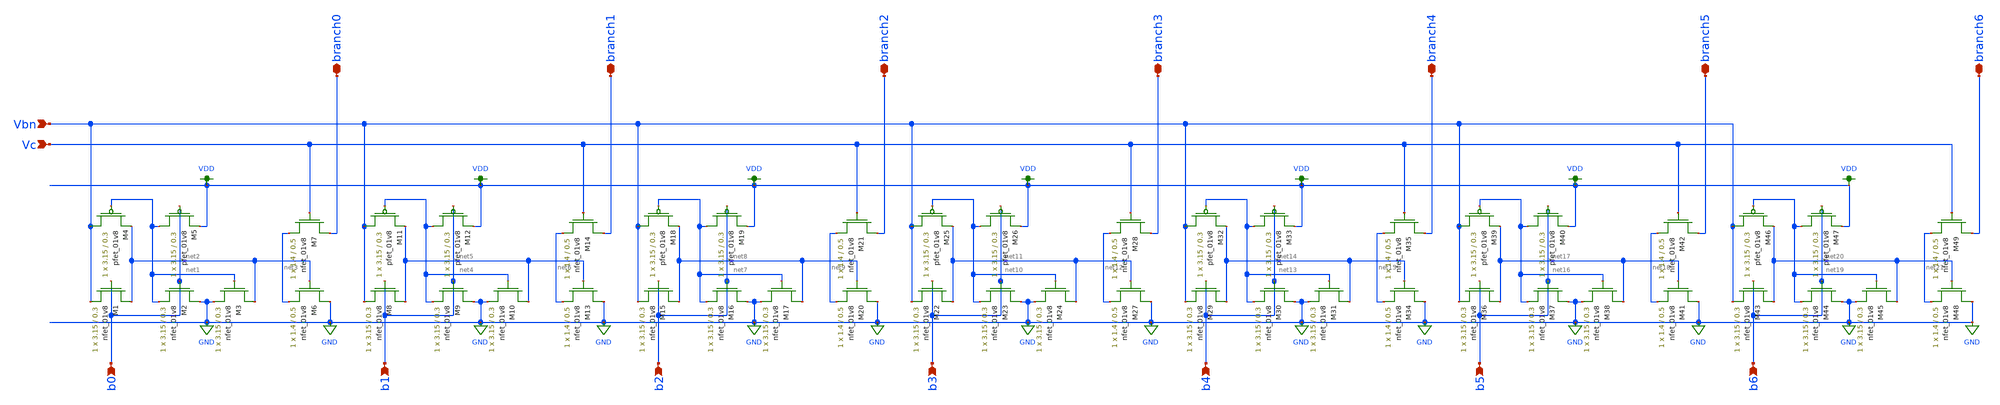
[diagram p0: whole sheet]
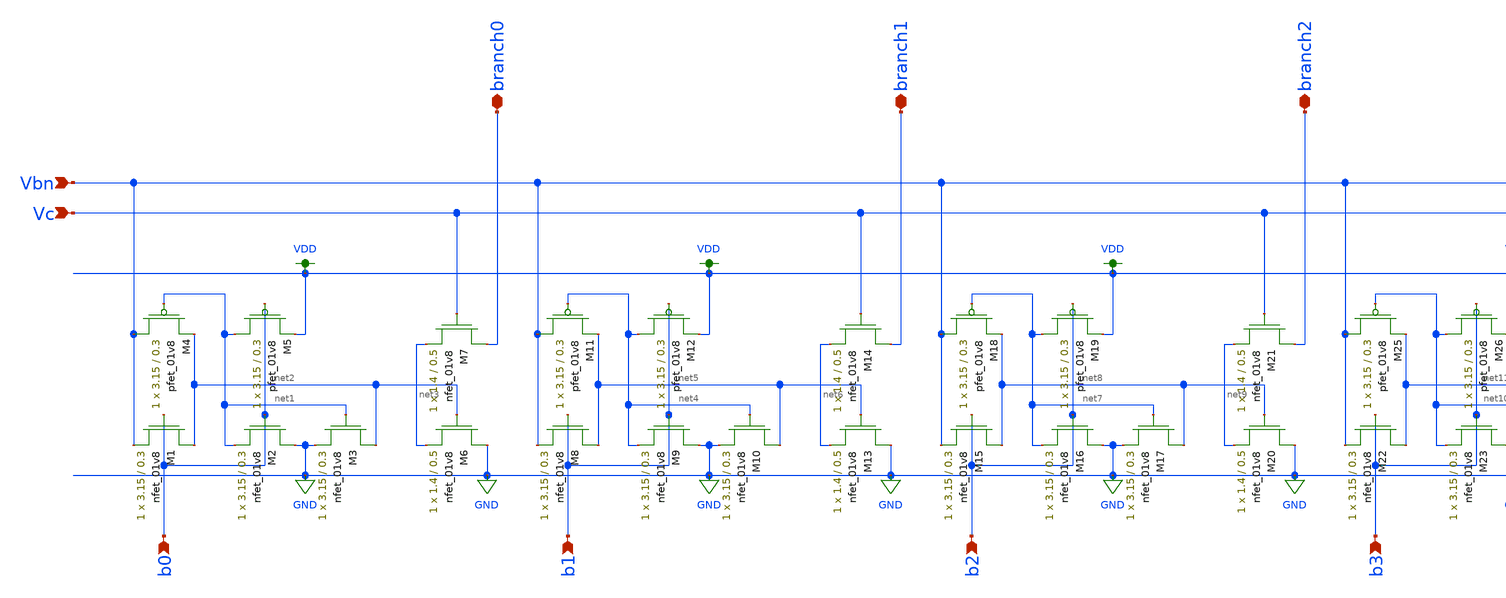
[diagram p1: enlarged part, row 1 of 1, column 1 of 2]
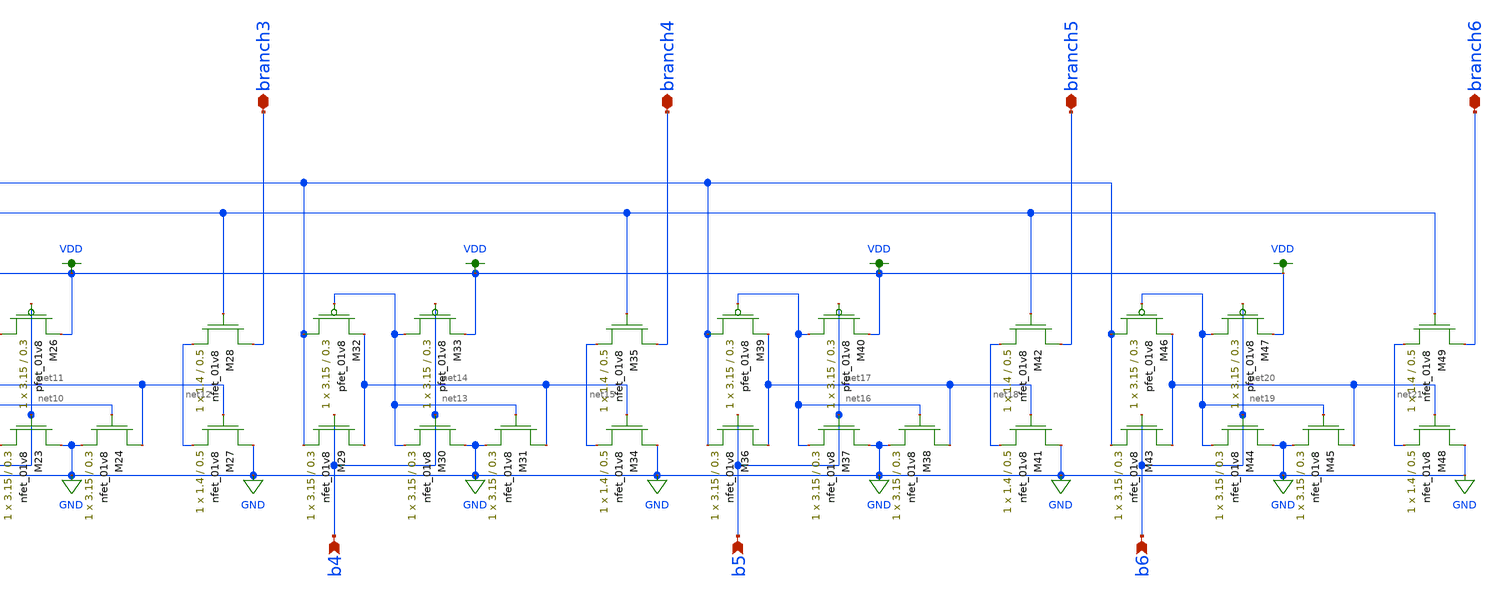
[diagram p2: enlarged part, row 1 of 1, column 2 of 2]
** sch_path: design-files/branchlogic.sch
**.subckt branchlogic Vc Vbn b0 branch0 b1 branch1 b2 branch2 b3 branch3 b4 branch4 b5 branch5 b6
*+ branch6
*.ipin Vc
*.ipin Vbn
*.ipin b0
*.iopin branch0
*.ipin b1
*.iopin branch1
*.ipin b2
*.iopin branch2
*.ipin b3
*.iopin branch3
*.ipin b4
*.iopin branch4
*.ipin b5
*.iopin branch5
*.ipin b6
*.iopin branch6
XM1 net2 b0 Vbn GND sky130_fd_pr__nfet_01v8 L=0.3 W=3.15 nf=1 ad='int((nf+1)/2) * W/nf * 0.29' as='int((nf+2)/2) * W/nf * 0.29'
+ pd='2*int((nf+1)/2) * (W/nf + 0.29)' ps='2*int((nf+2)/2) * (W/nf + 0.29)' nrd='0.29 / W' nrs='0.29 / W'
+ sa=0 sb=0 sd=0 mult=1 m=1
XM2 GND b0 net1 GND sky130_fd_pr__nfet_01v8 L=0.3 W=3.15 nf=1 ad='int((nf+1)/2) * W/nf * 0.29' as='int((nf+2)/2) * W/nf * 0.29'
+ pd='2*int((nf+1)/2) * (W/nf + 0.29)' ps='2*int((nf+2)/2) * (W/nf + 0.29)' nrd='0.29 / W' nrs='0.29 / W'
+ sa=0 sb=0 sd=0 mult=1 m=1
XM3 net2 net1 GND GND sky130_fd_pr__nfet_01v8 L=0.3 W=3.15 nf=1 ad='int((nf+1)/2) * W/nf * 0.29' as='int((nf+2)/2) * W/nf * 0.29'
+ pd='2*int((nf+1)/2) * (W/nf + 0.29)' ps='2*int((nf+2)/2) * (W/nf + 0.29)' nrd='0.29 / W' nrs='0.29 / W'
+ sa=0 sb=0 sd=0 mult=1 m=1
XM4 Vbn net1 net2 VDD sky130_fd_pr__pfet_01v8 L=0.3 W=3.15 nf=1 ad='int((nf+1)/2) * W/nf * 0.29' as='int((nf+2)/2) * W/nf * 0.29'
+ pd='2*int((nf+1)/2) * (W/nf + 0.29)' ps='2*int((nf+2)/2) * (W/nf + 0.29)' nrd='0.29 / W' nrs='0.29 / W'
+ sa=0 sb=0 sd=0 mult=1 m=1
XM5 net1 b0 VDD VDD sky130_fd_pr__pfet_01v8 L=0.3 W=3.15 nf=1 ad='int((nf+1)/2) * W/nf * 0.29' as='int((nf+2)/2) * W/nf * 0.29'
+ pd='2*int((nf+1)/2) * (W/nf + 0.29)' ps='2*int((nf+2)/2) * (W/nf + 0.29)' nrd='0.29 / W' nrs='0.29 / W'
+ sa=0 sb=0 sd=0 mult=1 m=1
XM6 GND net2 net3 GND sky130_fd_pr__nfet_01v8 L=0.5 W=1.4 nf=1 ad='int((nf+1)/2) * W/nf * 0.29' as='int((nf+2)/2) * W/nf * 0.29'
+ pd='2*int((nf+1)/2) * (W/nf + 0.29)' ps='2*int((nf+2)/2) * (W/nf + 0.29)' nrd='0.29 / W' nrs='0.29 / W'
+ sa=0 sb=0 sd=0 mult=1 m=1
XM7 branch0 Vc net3 GND sky130_fd_pr__nfet_01v8 L=0.5 W=1.4 nf=1 ad='int((nf+1)/2) * W/nf * 0.29' as='int((nf+2)/2) * W/nf * 0.29'
+ pd='2*int((nf+1)/2) * (W/nf + 0.29)' ps='2*int((nf+2)/2) * (W/nf + 0.29)' nrd='0.29 / W' nrs='0.29 / W'
+ sa=0 sb=0 sd=0 mult=1 m=1
XM8 net5 b1 Vbn GND sky130_fd_pr__nfet_01v8 L=0.3 W=3.15 nf=1 ad='int((nf+1)/2) * W/nf * 0.29' as='int((nf+2)/2) * W/nf * 0.29'
+ pd='2*int((nf+1)/2) * (W/nf + 0.29)' ps='2*int((nf+2)/2) * (W/nf + 0.29)' nrd='0.29 / W' nrs='0.29 / W'
+ sa=0 sb=0 sd=0 mult=1 m=1
XM9 GND b1 net4 GND sky130_fd_pr__nfet_01v8 L=0.3 W=3.15 nf=1 ad='int((nf+1)/2) * W/nf * 0.29' as='int((nf+2)/2) * W/nf * 0.29'
+ pd='2*int((nf+1)/2) * (W/nf + 0.29)' ps='2*int((nf+2)/2) * (W/nf + 0.29)' nrd='0.29 / W' nrs='0.29 / W'
+ sa=0 sb=0 sd=0 mult=1 m=1
XM10 net5 net4 GND GND sky130_fd_pr__nfet_01v8 L=0.3 W=3.15 nf=1 ad='int((nf+1)/2) * W/nf * 0.29' as='int((nf+2)/2) * W/nf * 0.29'
+ pd='2*int((nf+1)/2) * (W/nf + 0.29)' ps='2*int((nf+2)/2) * (W/nf + 0.29)' nrd='0.29 / W' nrs='0.29 / W'
+ sa=0 sb=0 sd=0 mult=1 m=1
XM11 Vbn net4 net5 VDD sky130_fd_pr__pfet_01v8 L=0.3 W=3.15 nf=1 ad='int((nf+1)/2) * W/nf * 0.29' as='int((nf+2)/2) * W/nf * 0.29'
+ pd='2*int((nf+1)/2) * (W/nf + 0.29)' ps='2*int((nf+2)/2) * (W/nf + 0.29)' nrd='0.29 / W' nrs='0.29 / W'
+ sa=0 sb=0 sd=0 mult=1 m=1
XM12 net4 b1 VDD VDD sky130_fd_pr__pfet_01v8 L=0.3 W=3.15 nf=1 ad='int((nf+1)/2) * W/nf * 0.29' as='int((nf+2)/2) * W/nf * 0.29'
+ pd='2*int((nf+1)/2) * (W/nf + 0.29)' ps='2*int((nf+2)/2) * (W/nf + 0.29)' nrd='0.29 / W' nrs='0.29 / W'
+ sa=0 sb=0 sd=0 mult=1 m=1
XM13 GND net5 net6 GND sky130_fd_pr__nfet_01v8 L=0.5 W=1.4 nf=1 ad='int((nf+1)/2) * W/nf * 0.29' as='int((nf+2)/2) * W/nf * 0.29'
+ pd='2*int((nf+1)/2) * (W/nf + 0.29)' ps='2*int((nf+2)/2) * (W/nf + 0.29)' nrd='0.29 / W' nrs='0.29 / W'
+ sa=0 sb=0 sd=0 mult=1 m=1
XM14 branch1 Vc net6 GND sky130_fd_pr__nfet_01v8 L=0.5 W=1.4 nf=1 ad='int((nf+1)/2) * W/nf * 0.29' as='int((nf+2)/2) * W/nf * 0.29'
+ pd='2*int((nf+1)/2) * (W/nf + 0.29)' ps='2*int((nf+2)/2) * (W/nf + 0.29)' nrd='0.29 / W' nrs='0.29 / W'
+ sa=0 sb=0 sd=0 mult=1 m=1
XM15 net8 b2 Vbn GND sky130_fd_pr__nfet_01v8 L=0.3 W=3.15 nf=1 ad='int((nf+1)/2) * W/nf * 0.29' as='int((nf+2)/2) * W/nf * 0.29'
+ pd='2*int((nf+1)/2) * (W/nf + 0.29)' ps='2*int((nf+2)/2) * (W/nf + 0.29)' nrd='0.29 / W' nrs='0.29 / W'
+ sa=0 sb=0 sd=0 mult=1 m=1
XM16 GND b2 net7 GND sky130_fd_pr__nfet_01v8 L=0.3 W=3.15 nf=1 ad='int((nf+1)/2) * W/nf * 0.29' as='int((nf+2)/2) * W/nf * 0.29'
+ pd='2*int((nf+1)/2) * (W/nf + 0.29)' ps='2*int((nf+2)/2) * (W/nf + 0.29)' nrd='0.29 / W' nrs='0.29 / W'
+ sa=0 sb=0 sd=0 mult=1 m=1
XM17 net8 net7 GND GND sky130_fd_pr__nfet_01v8 L=0.3 W=3.15 nf=1 ad='int((nf+1)/2) * W/nf * 0.29' as='int((nf+2)/2) * W/nf * 0.29'
+ pd='2*int((nf+1)/2) * (W/nf + 0.29)' ps='2*int((nf+2)/2) * (W/nf + 0.29)' nrd='0.29 / W' nrs='0.29 / W'
+ sa=0 sb=0 sd=0 mult=1 m=1
XM20 GND net8 net9 GND sky130_fd_pr__nfet_01v8 L=0.5 W=1.4 nf=1 ad='int((nf+1)/2) * W/nf * 0.29' as='int((nf+2)/2) * W/nf * 0.29'
+ pd='2*int((nf+1)/2) * (W/nf + 0.29)' ps='2*int((nf+2)/2) * (W/nf + 0.29)' nrd='0.29 / W' nrs='0.29 / W'
+ sa=0 sb=0 sd=0 mult=1 m=1
XM21 branch2 Vc net9 GND sky130_fd_pr__nfet_01v8 L=0.5 W=1.4 nf=1 ad='int((nf+1)/2) * W/nf * 0.29' as='int((nf+2)/2) * W/nf * 0.29'
+ pd='2*int((nf+1)/2) * (W/nf + 0.29)' ps='2*int((nf+2)/2) * (W/nf + 0.29)' nrd='0.29 / W' nrs='0.29 / W'
+ sa=0 sb=0 sd=0 mult=1 m=1
XM22 net11 b3 Vbn GND sky130_fd_pr__nfet_01v8 L=0.3 W=3.15 nf=1 ad='int((nf+1)/2) * W/nf * 0.29' as='int((nf+2)/2) * W/nf * 0.29'
+ pd='2*int((nf+1)/2) * (W/nf + 0.29)' ps='2*int((nf+2)/2) * (W/nf + 0.29)' nrd='0.29 / W' nrs='0.29 / W'
+ sa=0 sb=0 sd=0 mult=1 m=1
XM23 GND b3 net10 GND sky130_fd_pr__nfet_01v8 L=0.3 W=3.15 nf=1 ad='int((nf+1)/2) * W/nf * 0.29' as='int((nf+2)/2) * W/nf * 0.29'
+ pd='2*int((nf+1)/2) * (W/nf + 0.29)' ps='2*int((nf+2)/2) * (W/nf + 0.29)' nrd='0.29 / W' nrs='0.29 / W'
+ sa=0 sb=0 sd=0 mult=1 m=1
XM24 net11 net10 GND GND sky130_fd_pr__nfet_01v8 L=0.3 W=3.15 nf=1 ad='int((nf+1)/2) * W/nf * 0.29' as='int((nf+2)/2) * W/nf * 0.29'
+ pd='2*int((nf+1)/2) * (W/nf + 0.29)' ps='2*int((nf+2)/2) * (W/nf + 0.29)' nrd='0.29 / W' nrs='0.29 / W'
+ sa=0 sb=0 sd=0 mult=1 m=1
XM27 GND net11 net12 GND sky130_fd_pr__nfet_01v8 L=0.5 W=1.4 nf=1 ad='int((nf+1)/2) * W/nf * 0.29' as='int((nf+2)/2) * W/nf * 0.29'
+ pd='2*int((nf+1)/2) * (W/nf + 0.29)' ps='2*int((nf+2)/2) * (W/nf + 0.29)' nrd='0.29 / W' nrs='0.29 / W'
+ sa=0 sb=0 sd=0 mult=1 m=1
XM28 branch3 Vc net12 GND sky130_fd_pr__nfet_01v8 L=0.5 W=1.4 nf=1 ad='int((nf+1)/2) * W/nf * 0.29' as='int((nf+2)/2) * W/nf * 0.29'
+ pd='2*int((nf+1)/2) * (W/nf + 0.29)' ps='2*int((nf+2)/2) * (W/nf + 0.29)' nrd='0.29 / W' nrs='0.29 / W'
+ sa=0 sb=0 sd=0 mult=1 m=1
XM29 net14 b4 Vbn GND sky130_fd_pr__nfet_01v8 L=0.3 W=3.15 nf=1 ad='int((nf+1)/2) * W/nf * 0.29' as='int((nf+2)/2) * W/nf * 0.29'
+ pd='2*int((nf+1)/2) * (W/nf + 0.29)' ps='2*int((nf+2)/2) * (W/nf + 0.29)' nrd='0.29 / W' nrs='0.29 / W'
+ sa=0 sb=0 sd=0 mult=1 m=1
XM30 GND b4 net13 GND sky130_fd_pr__nfet_01v8 L=0.3 W=3.15 nf=1 ad='int((nf+1)/2) * W/nf * 0.29' as='int((nf+2)/2) * W/nf * 0.29'
+ pd='2*int((nf+1)/2) * (W/nf + 0.29)' ps='2*int((nf+2)/2) * (W/nf + 0.29)' nrd='0.29 / W' nrs='0.29 / W'
+ sa=0 sb=0 sd=0 mult=1 m=1
XM31 net14 net13 GND GND sky130_fd_pr__nfet_01v8 L=0.3 W=3.15 nf=1 ad='int((nf+1)/2) * W/nf * 0.29' as='int((nf+2)/2) * W/nf * 0.29'
+ pd='2*int((nf+1)/2) * (W/nf + 0.29)' ps='2*int((nf+2)/2) * (W/nf + 0.29)' nrd='0.29 / W' nrs='0.29 / W'
+ sa=0 sb=0 sd=0 mult=1 m=1
XM34 GND net14 net15 GND sky130_fd_pr__nfet_01v8 L=0.5 W=1.4 nf=1 ad='int((nf+1)/2) * W/nf * 0.29' as='int((nf+2)/2) * W/nf * 0.29'
+ pd='2*int((nf+1)/2) * (W/nf + 0.29)' ps='2*int((nf+2)/2) * (W/nf + 0.29)' nrd='0.29 / W' nrs='0.29 / W'
+ sa=0 sb=0 sd=0 mult=1 m=1
XM35 branch4 Vc net15 GND sky130_fd_pr__nfet_01v8 L=0.5 W=1.4 nf=1 ad='int((nf+1)/2) * W/nf * 0.29' as='int((nf+2)/2) * W/nf * 0.29'
+ pd='2*int((nf+1)/2) * (W/nf + 0.29)' ps='2*int((nf+2)/2) * (W/nf + 0.29)' nrd='0.29 / W' nrs='0.29 / W'
+ sa=0 sb=0 sd=0 mult=1 m=1
XM36 net17 b5 Vbn GND sky130_fd_pr__nfet_01v8 L=0.3 W=3.15 nf=1 ad='int((nf+1)/2) * W/nf * 0.29' as='int((nf+2)/2) * W/nf * 0.29'
+ pd='2*int((nf+1)/2) * (W/nf + 0.29)' ps='2*int((nf+2)/2) * (W/nf + 0.29)' nrd='0.29 / W' nrs='0.29 / W'
+ sa=0 sb=0 sd=0 mult=1 m=1
XM37 GND b5 net16 GND sky130_fd_pr__nfet_01v8 L=0.3 W=3.15 nf=1 ad='int((nf+1)/2) * W/nf * 0.29' as='int((nf+2)/2) * W/nf * 0.29'
+ pd='2*int((nf+1)/2) * (W/nf + 0.29)' ps='2*int((nf+2)/2) * (W/nf + 0.29)' nrd='0.29 / W' nrs='0.29 / W'
+ sa=0 sb=0 sd=0 mult=1 m=1
XM38 net17 net16 GND GND sky130_fd_pr__nfet_01v8 L=0.3 W=3.15 nf=1 ad='int((nf+1)/2) * W/nf * 0.29' as='int((nf+2)/2) * W/nf * 0.29'
+ pd='2*int((nf+1)/2) * (W/nf + 0.29)' ps='2*int((nf+2)/2) * (W/nf + 0.29)' nrd='0.29 / W' nrs='0.29 / W'
+ sa=0 sb=0 sd=0 mult=1 m=1
XM41 GND net17 net18 GND sky130_fd_pr__nfet_01v8 L=0.5 W=1.4 nf=1 ad='int((nf+1)/2) * W/nf * 0.29' as='int((nf+2)/2) * W/nf * 0.29'
+ pd='2*int((nf+1)/2) * (W/nf + 0.29)' ps='2*int((nf+2)/2) * (W/nf + 0.29)' nrd='0.29 / W' nrs='0.29 / W'
+ sa=0 sb=0 sd=0 mult=1 m=1
XM42 branch5 Vc net18 GND sky130_fd_pr__nfet_01v8 L=0.5 W=1.4 nf=1 ad='int((nf+1)/2) * W/nf * 0.29' as='int((nf+2)/2) * W/nf * 0.29'
+ pd='2*int((nf+1)/2) * (W/nf + 0.29)' ps='2*int((nf+2)/2) * (W/nf + 0.29)' nrd='0.29 / W' nrs='0.29 / W'
+ sa=0 sb=0 sd=0 mult=1 m=1
XM43 net20 b6 Vbn GND sky130_fd_pr__nfet_01v8 L=0.3 W=3.15 nf=1 ad='int((nf+1)/2) * W/nf * 0.29' as='int((nf+2)/2) * W/nf * 0.29'
+ pd='2*int((nf+1)/2) * (W/nf + 0.29)' ps='2*int((nf+2)/2) * (W/nf + 0.29)' nrd='0.29 / W' nrs='0.29 / W'
+ sa=0 sb=0 sd=0 mult=1 m=1
XM44 GND b6 net19 GND sky130_fd_pr__nfet_01v8 L=0.3 W=3.15 nf=1 ad='int((nf+1)/2) * W/nf * 0.29' as='int((nf+2)/2) * W/nf * 0.29'
+ pd='2*int((nf+1)/2) * (W/nf + 0.29)' ps='2*int((nf+2)/2) * (W/nf + 0.29)' nrd='0.29 / W' nrs='0.29 / W'
+ sa=0 sb=0 sd=0 mult=1 m=1
XM45 net20 net19 GND GND sky130_fd_pr__nfet_01v8 L=0.3 W=3.15 nf=1 ad='int((nf+1)/2) * W/nf * 0.29' as='int((nf+2)/2) * W/nf * 0.29'
+ pd='2*int((nf+1)/2) * (W/nf + 0.29)' ps='2*int((nf+2)/2) * (W/nf + 0.29)' nrd='0.29 / W' nrs='0.29 / W'
+ sa=0 sb=0 sd=0 mult=1 m=1
XM48 GND net20 net21 GND sky130_fd_pr__nfet_01v8 L=0.5 W=1.4 nf=1 ad='int((nf+1)/2) * W/nf * 0.29' as='int((nf+2)/2) * W/nf * 0.29'
+ pd='2*int((nf+1)/2) * (W/nf + 0.29)' ps='2*int((nf+2)/2) * (W/nf + 0.29)' nrd='0.29 / W' nrs='0.29 / W'
+ sa=0 sb=0 sd=0 mult=1 m=1
XM49 branch6 Vc net21 GND sky130_fd_pr__nfet_01v8 L=0.5 W=1.4 nf=1 ad='int((nf+1)/2) * W/nf * 0.29' as='int((nf+2)/2) * W/nf * 0.29'
+ pd='2*int((nf+1)/2) * (W/nf + 0.29)' ps='2*int((nf+2)/2) * (W/nf + 0.29)' nrd='0.29 / W' nrs='0.29 / W'
+ sa=0 sb=0 sd=0 mult=1 m=1
XM18 Vbn net7 net8 VDD sky130_fd_pr__pfet_01v8 L=0.3 W=3.15 nf=1 ad='int((nf+1)/2) * W/nf * 0.29' as='int((nf+2)/2) * W/nf * 0.29'
+ pd='2*int((nf+1)/2) * (W/nf + 0.29)' ps='2*int((nf+2)/2) * (W/nf + 0.29)' nrd='0.29 / W' nrs='0.29 / W'
+ sa=0 sb=0 sd=0 mult=1 m=1
XM19 net7 b2 VDD VDD sky130_fd_pr__pfet_01v8 L=0.3 W=3.15 nf=1 ad='int((nf+1)/2) * W/nf * 0.29' as='int((nf+2)/2) * W/nf * 0.29'
+ pd='2*int((nf+1)/2) * (W/nf + 0.29)' ps='2*int((nf+2)/2) * (W/nf + 0.29)' nrd='0.29 / W' nrs='0.29 / W'
+ sa=0 sb=0 sd=0 mult=1 m=1
XM25 Vbn net10 net11 VDD sky130_fd_pr__pfet_01v8 L=0.3 W=3.15 nf=1 ad='int((nf+1)/2) * W/nf * 0.29' as='int((nf+2)/2) * W/nf * 0.29'
+ pd='2*int((nf+1)/2) * (W/nf + 0.29)' ps='2*int((nf+2)/2) * (W/nf + 0.29)' nrd='0.29 / W' nrs='0.29 / W'
+ sa=0 sb=0 sd=0 mult=1 m=1
XM26 net10 b3 VDD VDD sky130_fd_pr__pfet_01v8 L=0.3 W=3.15 nf=1 ad='int((nf+1)/2) * W/nf * 0.29' as='int((nf+2)/2) * W/nf * 0.29'
+ pd='2*int((nf+1)/2) * (W/nf + 0.29)' ps='2*int((nf+2)/2) * (W/nf + 0.29)' nrd='0.29 / W' nrs='0.29 / W'
+ sa=0 sb=0 sd=0 mult=1 m=1
XM32 Vbn net13 net14 VDD sky130_fd_pr__pfet_01v8 L=0.3 W=3.15 nf=1 ad='int((nf+1)/2) * W/nf * 0.29' as='int((nf+2)/2) * W/nf * 0.29'
+ pd='2*int((nf+1)/2) * (W/nf + 0.29)' ps='2*int((nf+2)/2) * (W/nf + 0.29)' nrd='0.29 / W' nrs='0.29 / W'
+ sa=0 sb=0 sd=0 mult=1 m=1
XM33 net13 b4 VDD VDD sky130_fd_pr__pfet_01v8 L=0.3 W=3.15 nf=1 ad='int((nf+1)/2) * W/nf * 0.29' as='int((nf+2)/2) * W/nf * 0.29'
+ pd='2*int((nf+1)/2) * (W/nf + 0.29)' ps='2*int((nf+2)/2) * (W/nf + 0.29)' nrd='0.29 / W' nrs='0.29 / W'
+ sa=0 sb=0 sd=0 mult=1 m=1
XM39 Vbn net16 net17 VDD sky130_fd_pr__pfet_01v8 L=0.3 W=3.15 nf=1 ad='int((nf+1)/2) * W/nf * 0.29' as='int((nf+2)/2) * W/nf * 0.29'
+ pd='2*int((nf+1)/2) * (W/nf + 0.29)' ps='2*int((nf+2)/2) * (W/nf + 0.29)' nrd='0.29 / W' nrs='0.29 / W'
+ sa=0 sb=0 sd=0 mult=1 m=1
XM40 net16 b5 VDD VDD sky130_fd_pr__pfet_01v8 L=0.3 W=3.15 nf=1 ad='int((nf+1)/2) * W/nf * 0.29' as='int((nf+2)/2) * W/nf * 0.29'
+ pd='2*int((nf+1)/2) * (W/nf + 0.29)' ps='2*int((nf+2)/2) * (W/nf + 0.29)' nrd='0.29 / W' nrs='0.29 / W'
+ sa=0 sb=0 sd=0 mult=1 m=1
XM46 Vbn net19 net20 VDD sky130_fd_pr__pfet_01v8 L=0.3 W=3.15 nf=1 ad='int((nf+1)/2) * W/nf * 0.29' as='int((nf+2)/2) * W/nf * 0.29'
+ pd='2*int((nf+1)/2) * (W/nf + 0.29)' ps='2*int((nf+2)/2) * (W/nf + 0.29)' nrd='0.29 / W' nrs='0.29 / W'
+ sa=0 sb=0 sd=0 mult=1 m=1
XM47 net19 b6 VDD VDD sky130_fd_pr__pfet_01v8 L=0.3 W=3.15 nf=1 ad='int((nf+1)/2) * W/nf * 0.29' as='int((nf+2)/2) * W/nf * 0.29'
+ pd='2*int((nf+1)/2) * (W/nf + 0.29)' ps='2*int((nf+2)/2) * (W/nf + 0.29)' nrd='0.29 / W' nrs='0.29 / W'
+ sa=0 sb=0 sd=0 mult=1 m=1
**.ends
.GLOBAL GND
.GLOBAL VDD
.end
